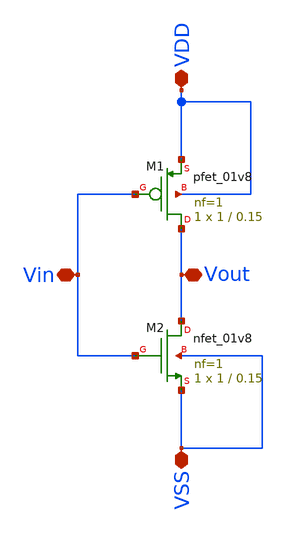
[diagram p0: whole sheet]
** sch_path: TT/inverter_ro.sch
**.subckt inverter_ro VDD VSS Vout Vin
*.iopin VDD
*.iopin VSS
*.iopin Vout
*.iopin Vin
XM1 Vout Vin VDD VDD sky130_fd_pr__pfet_01v8 L=0.15 W=1 nf=1 ad='int((nf+1)/2) * W/nf * 0.29' as='int((nf+2)/2) * W/nf * 0.29'
+ pd='2*int((nf+1)/2) * (W/nf + 0.29)' ps='2*int((nf+2)/2) * (W/nf + 0.29)' nrd='0.29 / W' nrs='0.29 / W'
+ sa=0 sb=0 sd=0 mult=1 m=1
XM2 Vout Vin VSS VSS sky130_fd_pr__nfet_01v8 L=0.15 W=1 nf=1 ad='int((nf+1)/2) * W/nf * 0.29' as='int((nf+2)/2) * W/nf * 0.29'
+ pd='2*int((nf+1)/2) * (W/nf + 0.29)' ps='2*int((nf+2)/2) * (W/nf + 0.29)' nrd='0.29 / W' nrs='0.29 / W'
+ sa=0 sb=0 sd=0 mult=1 m=1
**.ends
.end
